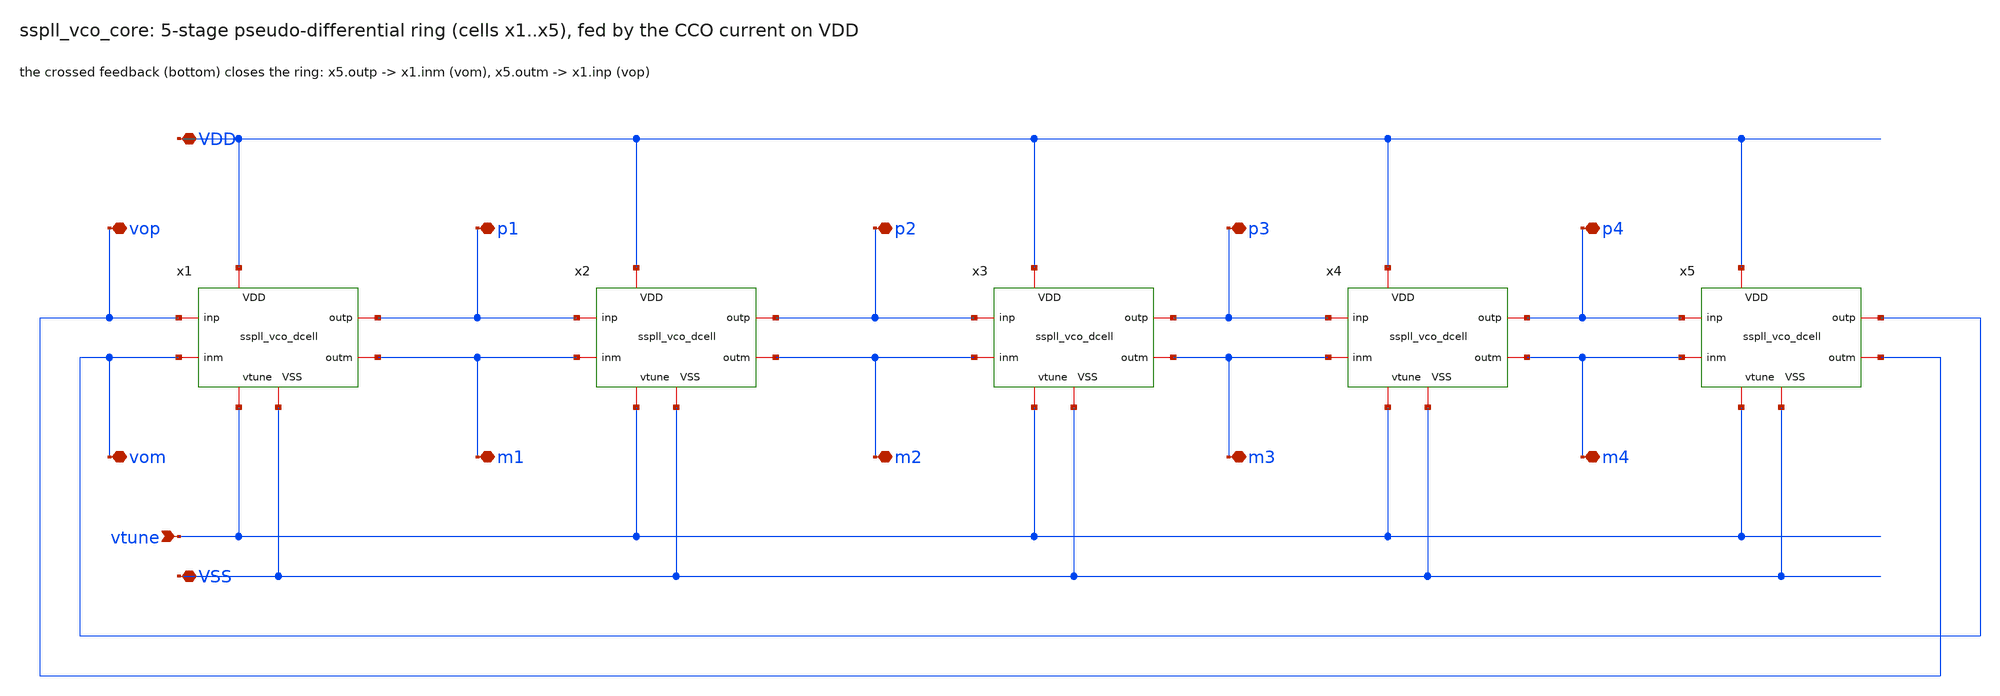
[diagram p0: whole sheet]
** sch_path: xschem/vco/sspll_vco_core.sch
**.subckt sspll_vco_core VDD vtune VSS p1 m1 p2 m2 p3 m3 p4 m4 vop vom
*.iopin VDD
*.ipin vtune
*.iopin VSS
*.iopin p1
*.iopin m1
*.iopin p2
*.iopin m2
*.iopin p3
*.iopin m3
*.iopin p4
*.iopin m4
*.iopin vop
*.iopin vom
x1 vop vom p1 m1 VDD vtune VSS sspll_vco_dcell
x2 p1 m1 p2 m2 VDD vtune VSS sspll_vco_dcell
x3 p2 m2 p3 m3 VDD vtune VSS sspll_vco_dcell
x4 p3 m3 p4 m4 VDD vtune VSS sspll_vco_dcell
x5 p4 m4 vom vop VDD vtune VSS sspll_vco_dcell
**.ends

* expanding   symbol:  sspll_vco_dcell.sym # of pins=7
** sym_path: xschem/vco/sspll_vco_dcell.sym
** sch_path: xschem/vco/sspll_vco_dcell.sch
.subckt sspll_vco_dcell inp inm outp outm VDD vtune VSS
*.iopin VDD
*.iopin VSS
*.ipin vtune
*.ipin inp
*.ipin inm
*.opin outm
*.opin outp
XXP1 outm inp VDD VDD sky130_fd_pr__pfet_01v8 L=0.15 W=12 nf=4 ad='int((nf+1)/2) * W/nf * 0.29' as='int((nf+2)/2) * W/nf * 0.29'
+ pd='2*int((nf+1)/2) * (W/nf + 0.29)' ps='2*int((nf+2)/2) * (W/nf + 0.29)' nrd='0.29 / W' nrs='0.29 / W'
+ sa=0 sb=0 sd=0 mult=1 m=1
XXN1 outm inp VSS VSS sky130_fd_pr__nfet_01v8 L=0.15 W=6 nf=2 ad='int((nf+1)/2) * W/nf * 0.29' as='int((nf+2)/2) * W/nf * 0.29'
+ pd='2*int((nf+1)/2) * (W/nf + 0.29)' ps='2*int((nf+2)/2) * (W/nf + 0.29)' nrd='0.29 / W' nrs='0.29 / W'
+ sa=0 sb=0 sd=0 mult=1 m=1
XXS1 outm vtune net1 VSS sky130_fd_pr__nfet_01v8 L=0.15 W=2.25 nf=1 ad='int((nf+1)/2) * W/nf * 0.29'
+ as='int((nf+2)/2) * W/nf * 0.29' pd='2*int((nf+1)/2) * (W/nf + 0.29)' ps='2*int((nf+2)/2) * (W/nf + 0.29)'
+ nrd='0.29 / W' nrs='0.29 / W' sa=0 sb=0 sd=0 mult=1 m=1
XXC1 VSS net1 VSS VSS sky130_fd_pr__nfet_01v8 L=0.5 W=4.5 nf=1 ad='int((nf+1)/2) * W/nf * 0.29' as='int((nf+2)/2) * W/nf * 0.29'
+ pd='2*int((nf+1)/2) * (W/nf + 0.29)' ps='2*int((nf+2)/2) * (W/nf + 0.29)' nrd='0.29 / W' nrs='0.29 / W'
+ sa=0 sb=0 sd=0 mult=1 m=1
XXP2 outp inm VDD VDD sky130_fd_pr__pfet_01v8 L=0.15 W=12 nf=4 ad='int((nf+1)/2) * W/nf * 0.29' as='int((nf+2)/2) * W/nf * 0.29'
+ pd='2*int((nf+1)/2) * (W/nf + 0.29)' ps='2*int((nf+2)/2) * (W/nf + 0.29)' nrd='0.29 / W' nrs='0.29 / W'
+ sa=0 sb=0 sd=0 mult=1 m=1
XXN2 outp inm VSS VSS sky130_fd_pr__nfet_01v8 L=0.15 W=6 nf=2 ad='int((nf+1)/2) * W/nf * 0.29' as='int((nf+2)/2) * W/nf * 0.29'
+ pd='2*int((nf+1)/2) * (W/nf + 0.29)' ps='2*int((nf+2)/2) * (W/nf + 0.29)' nrd='0.29 / W' nrs='0.29 / W'
+ sa=0 sb=0 sd=0 mult=1 m=1
XXS2 outp vtune net2 VSS sky130_fd_pr__nfet_01v8 L=0.15 W=2.25 nf=1 ad='int((nf+1)/2) * W/nf * 0.29'
+ as='int((nf+2)/2) * W/nf * 0.29' pd='2*int((nf+1)/2) * (W/nf + 0.29)' ps='2*int((nf+2)/2) * (W/nf + 0.29)'
+ nrd='0.29 / W' nrs='0.29 / W' sa=0 sb=0 sd=0 mult=1 m=1
XXC2 VSS net2 VSS VSS sky130_fd_pr__nfet_01v8 L=0.5 W=4.5 nf=1 ad='int((nf+1)/2) * W/nf * 0.29' as='int((nf+2)/2) * W/nf * 0.29'
+ pd='2*int((nf+1)/2) * (W/nf + 0.29)' ps='2*int((nf+2)/2) * (W/nf + 0.29)' nrd='0.29 / W' nrs='0.29 / W'
+ sa=0 sb=0 sd=0 mult=1 m=1
XXT1N inp VDD outp VSS sky130_fd_pr__nfet_01v8 L=0.15 W=0.63 nf=1 ad='int((nf+1)/2) * W/nf * 0.29' as='int((nf+2)/2) * W/nf * 0.29'
+ pd='2*int((nf+1)/2) * (W/nf + 0.29)' ps='2*int((nf+2)/2) * (W/nf + 0.29)' nrd='0.29 / W' nrs='0.29 / W'
+ sa=0 sb=0 sd=0 mult=1 m=1
XXT1P outp VSS inp VDD sky130_fd_pr__pfet_01v8 L=0.15 W=0.63 nf=1 ad='int((nf+1)/2) * W/nf * 0.29' as='int((nf+2)/2) * W/nf * 0.29'
+ pd='2*int((nf+1)/2) * (W/nf + 0.29)' ps='2*int((nf+2)/2) * (W/nf + 0.29)' nrd='0.29 / W' nrs='0.29 / W'
+ sa=0 sb=0 sd=0 mult=1 m=1
XXT2N inm VDD outm VSS sky130_fd_pr__nfet_01v8 L=0.15 W=0.63 nf=1 ad='int((nf+1)/2) * W/nf * 0.29' as='int((nf+2)/2) * W/nf * 0.29'
+ pd='2*int((nf+1)/2) * (W/nf + 0.29)' ps='2*int((nf+2)/2) * (W/nf + 0.29)' nrd='0.29 / W' nrs='0.29 / W'
+ sa=0 sb=0 sd=0 mult=1 m=1
XXT2P outm VSS inm VDD sky130_fd_pr__pfet_01v8 L=0.15 W=0.63 nf=1 ad='int((nf+1)/2) * W/nf * 0.29' as='int((nf+2)/2) * W/nf * 0.29'
+ pd='2*int((nf+1)/2) * (W/nf + 0.29)' ps='2*int((nf+2)/2) * (W/nf + 0.29)' nrd='0.29 / W' nrs='0.29 / W'
+ sa=0 sb=0 sd=0 mult=1 m=1
.ends

.end
